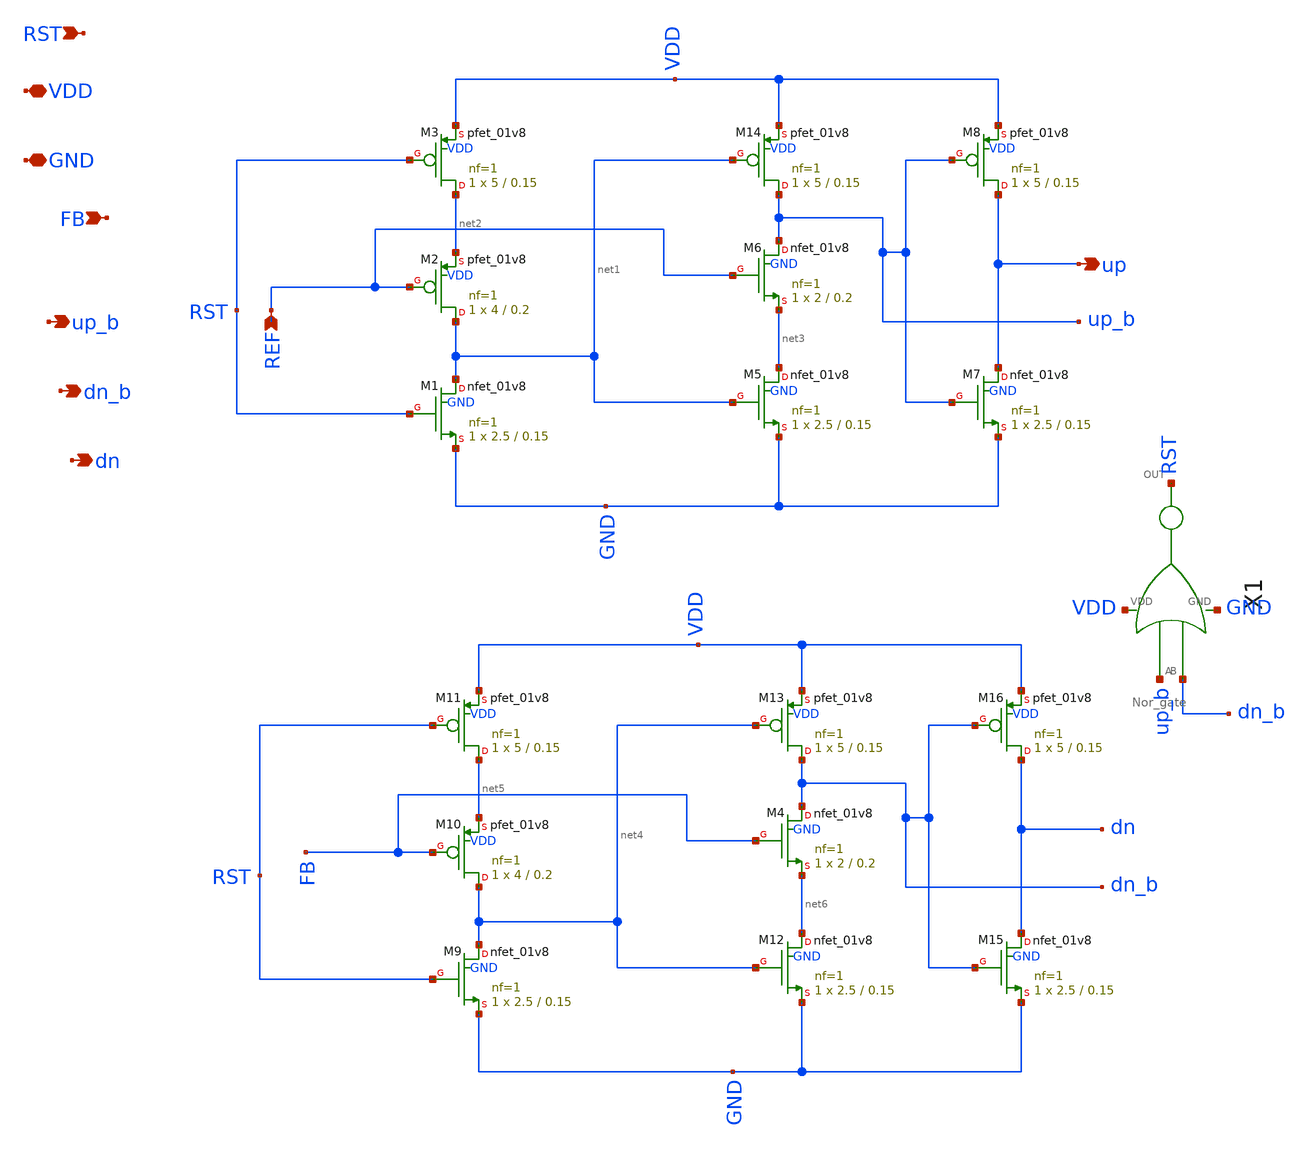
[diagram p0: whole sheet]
** sch_path: pll/pfd_cp_lf_lib/coventional_pfd/xschem/conventional_pfd.sch
**.subckt conventional_pfd REF RST VDD GND FB up up_b dn_b dn
*.ipin REF
*.ipin RST
*.iopin VDD
*.iopin GND
*.ipin FB
*.opin up
*.opin up_b
*.opin dn_b
*.opin dn
XM1 net1 RST GND GND sky130_fd_pr__nfet_01v8 L=0.15 W=2.5 nf=1 ad='int((nf+1)/2) * W/nf * 0.29' as='int((nf+2)/2) * W/nf * 0.29'
+ pd='2*int((nf+1)/2) * (W/nf + 0.29)' ps='2*int((nf+2)/2) * (W/nf + 0.29)' nrd='0.29 / W' nrs='0.29 / W'
+ sa=0 sb=0 sd=0 mult=1 m=1
XM2 net1 REF net2 VDD sky130_fd_pr__pfet_01v8 L=0.2 W=4 nf=1 ad='int((nf+1)/2) * W/nf * 0.29' as='int((nf+2)/2) * W/nf * 0.29'
+ pd='2*int((nf+1)/2) * (W/nf + 0.29)' ps='2*int((nf+2)/2) * (W/nf + 0.29)' nrd='0.29 / W' nrs='0.29 / W'
+ sa=0 sb=0 sd=0 mult=1 m=1
XM3 net2 RST VDD VDD sky130_fd_pr__pfet_01v8 L=0.15 W=5 nf=1 ad='int((nf+1)/2) * W/nf * 0.29' as='int((nf+2)/2) * W/nf * 0.29'
+ pd='2*int((nf+1)/2) * (W/nf + 0.29)' ps='2*int((nf+2)/2) * (W/nf + 0.29)' nrd='0.29 / W' nrs='0.29 / W'
+ sa=0 sb=0 sd=0 mult=1 m=1
XM10 net4 FB net5 VDD sky130_fd_pr__pfet_01v8 L=0.2 W=4 nf=1 ad='int((nf+1)/2) * W/nf * 0.29' as='int((nf+2)/2) * W/nf * 0.29'
+ pd='2*int((nf+1)/2) * (W/nf + 0.29)' ps='2*int((nf+2)/2) * (W/nf + 0.29)' nrd='0.29 / W' nrs='0.29 / W'
+ sa=0 sb=0 sd=0 mult=1 m=1
X1 up_b dn_b VDD GND RST Nor_gate
XM4 dn_b FB net6 GND sky130_fd_pr__nfet_01v8 L=0.2 W=2 nf=1 ad='int((nf+1)/2) * W/nf * 0.29' as='int((nf+2)/2) * W/nf * 0.29'
+ pd='2*int((nf+1)/2) * (W/nf + 0.29)' ps='2*int((nf+2)/2) * (W/nf + 0.29)' nrd='0.29 / W' nrs='0.29 / W'
+ sa=0 sb=0 sd=0 mult=1 m=1
XM6 up_b REF net3 GND sky130_fd_pr__nfet_01v8 L=0.2 W=2 nf=1 ad='int((nf+1)/2) * W/nf * 0.29' as='int((nf+2)/2) * W/nf * 0.29'
+ pd='2*int((nf+1)/2) * (W/nf + 0.29)' ps='2*int((nf+2)/2) * (W/nf + 0.29)' nrd='0.29 / W' nrs='0.29 / W'
+ sa=0 sb=0 sd=0 mult=1 m=1
XM5 net3 net1 GND GND sky130_fd_pr__nfet_01v8 L=0.15 W=2.5 nf=1 ad='int((nf+1)/2) * W/nf * 0.29' as='int((nf+2)/2) * W/nf * 0.29'
+ pd='2*int((nf+1)/2) * (W/nf + 0.29)' ps='2*int((nf+2)/2) * (W/nf + 0.29)' nrd='0.29 / W' nrs='0.29 / W'
+ sa=0 sb=0 sd=0 mult=1 m=1
XM14 up_b net1 VDD VDD sky130_fd_pr__pfet_01v8 L=0.15 W=5 nf=1 ad='int((nf+1)/2) * W/nf * 0.29' as='int((nf+2)/2) * W/nf * 0.29'
+ pd='2*int((nf+1)/2) * (W/nf + 0.29)' ps='2*int((nf+2)/2) * (W/nf + 0.29)' nrd='0.29 / W' nrs='0.29 / W'
+ sa=0 sb=0 sd=0 mult=1 m=1
XM9 net4 RST GND GND sky130_fd_pr__nfet_01v8 L=0.15 W=2.5 nf=1 ad='int((nf+1)/2) * W/nf * 0.29' as='int((nf+2)/2) * W/nf * 0.29'
+ pd='2*int((nf+1)/2) * (W/nf + 0.29)' ps='2*int((nf+2)/2) * (W/nf + 0.29)' nrd='0.29 / W' nrs='0.29 / W'
+ sa=0 sb=0 sd=0 mult=1 m=1
XM11 net5 RST VDD VDD sky130_fd_pr__pfet_01v8 L=0.15 W=5 nf=1 ad='int((nf+1)/2) * W/nf * 0.29' as='int((nf+2)/2) * W/nf * 0.29'
+ pd='2*int((nf+1)/2) * (W/nf + 0.29)' ps='2*int((nf+2)/2) * (W/nf + 0.29)' nrd='0.29 / W' nrs='0.29 / W'
+ sa=0 sb=0 sd=0 mult=1 m=1
XM12 net6 net4 GND GND sky130_fd_pr__nfet_01v8 L=0.15 W=2.5 nf=1 ad='int((nf+1)/2) * W/nf * 0.29' as='int((nf+2)/2) * W/nf * 0.29'
+ pd='2*int((nf+1)/2) * (W/nf + 0.29)' ps='2*int((nf+2)/2) * (W/nf + 0.29)' nrd='0.29 / W' nrs='0.29 / W'
+ sa=0 sb=0 sd=0 mult=1 m=1
XM13 dn_b net4 VDD VDD sky130_fd_pr__pfet_01v8 L=0.15 W=5 nf=1 ad='int((nf+1)/2) * W/nf * 0.29' as='int((nf+2)/2) * W/nf * 0.29'
+ pd='2*int((nf+1)/2) * (W/nf + 0.29)' ps='2*int((nf+2)/2) * (W/nf + 0.29)' nrd='0.29 / W' nrs='0.29 / W'
+ sa=0 sb=0 sd=0 mult=1 m=1
XM15 dn dn_b GND GND sky130_fd_pr__nfet_01v8 L=0.15 W=2.5 nf=1 ad='int((nf+1)/2) * W/nf * 0.29' as='int((nf+2)/2) * W/nf * 0.29'
+ pd='2*int((nf+1)/2) * (W/nf + 0.29)' ps='2*int((nf+2)/2) * (W/nf + 0.29)' nrd='0.29 / W' nrs='0.29 / W'
+ sa=0 sb=0 sd=0 mult=1 m=1
XM16 dn dn_b VDD VDD sky130_fd_pr__pfet_01v8 L=0.15 W=5 nf=1 ad='int((nf+1)/2) * W/nf * 0.29' as='int((nf+2)/2) * W/nf * 0.29'
+ pd='2*int((nf+1)/2) * (W/nf + 0.29)' ps='2*int((nf+2)/2) * (W/nf + 0.29)' nrd='0.29 / W' nrs='0.29 / W'
+ sa=0 sb=0 sd=0 mult=1 m=1
XM7 up up_b GND GND sky130_fd_pr__nfet_01v8 L=0.15 W=2.5 nf=1 ad='int((nf+1)/2) * W/nf * 0.29' as='int((nf+2)/2) * W/nf * 0.29'
+ pd='2*int((nf+1)/2) * (W/nf + 0.29)' ps='2*int((nf+2)/2) * (W/nf + 0.29)' nrd='0.29 / W' nrs='0.29 / W'
+ sa=0 sb=0 sd=0 mult=1 m=1
XM8 up up_b VDD VDD sky130_fd_pr__pfet_01v8 L=0.15 W=5 nf=1 ad='int((nf+1)/2) * W/nf * 0.29' as='int((nf+2)/2) * W/nf * 0.29'
+ pd='2*int((nf+1)/2) * (W/nf + 0.29)' ps='2*int((nf+2)/2) * (W/nf + 0.29)' nrd='0.29 / W' nrs='0.29 / W'
+ sa=0 sb=0 sd=0 mult=1 m=1
**.ends

* expanding   symbol:  Nor_gate.sym # of pins=5
** sym_path: pll/pfd_cp_lf_lib/coventional_pfd/xschem/Nor_gate.sym
** sch_path: pll/pfd_cp_lf_lib/coventional_pfd/xschem/Nor_gate.sch
.subckt Nor_gate A B VDD GND OUT
*.ipin A
*.ipin B
*.iopin VDD
*.iopin GND
*.opin OUT
XM9 OUT A GND GND sky130_fd_pr__nfet_01v8 L=0.2 W=2 nf=1 ad='int((nf+1)/2) * W/nf * 0.29' as='int((nf+2)/2) * W/nf * 0.29'
+ pd='2*int((nf+1)/2) * (W/nf + 0.29)' ps='2*int((nf+2)/2) * (W/nf + 0.29)' nrd='0.29 / W' nrs='0.29 / W'
+ sa=0 sb=0 sd=0 mult=1 m=1
XM1 OUT B GND GND sky130_fd_pr__nfet_01v8 L=0.2 W=2 nf=1 ad='int((nf+1)/2) * W/nf * 0.29' as='int((nf+2)/2) * W/nf * 0.29'
+ pd='2*int((nf+1)/2) * (W/nf + 0.29)' ps='2*int((nf+2)/2) * (W/nf + 0.29)' nrd='0.29 / W' nrs='0.29 / W'
+ sa=0 sb=0 sd=0 mult=1 m=1
XM13 net1 A VDD VDD sky130_fd_pr__pfet_01v8 L=0.2 W=4 nf=1 ad='int((nf+1)/2) * W/nf * 0.29' as='int((nf+2)/2) * W/nf * 0.29'
+ pd='2*int((nf+1)/2) * (W/nf + 0.29)' ps='2*int((nf+2)/2) * (W/nf + 0.29)' nrd='0.29 / W' nrs='0.29 / W'
+ sa=0 sb=0 sd=0 mult=1 m=1
XM14 OUT B net1 VDD sky130_fd_pr__pfet_01v8 L=0.2 W=4 nf=1 ad='int((nf+1)/2) * W/nf * 0.29' as='int((nf+2)/2) * W/nf * 0.29'
+ pd='2*int((nf+1)/2) * (W/nf + 0.29)' ps='2*int((nf+2)/2) * (W/nf + 0.29)' nrd='0.29 / W' nrs='0.29 / W'
+ sa=0 sb=0 sd=0 mult=1 m=1
.ends

.end
